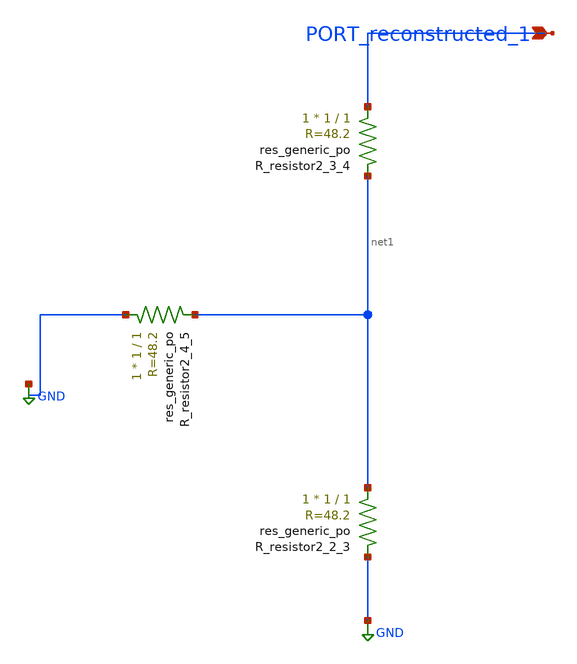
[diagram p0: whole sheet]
** sch_path: schematics/AMSNet/94.sch
**.subckt 94 PORT_reconstructed_1
*.ipin PORT_reconstructed_1
XR_resistor2_2_3 net1 GND sky130_fd_pr__res_generic_po W=1 L=1 m=1
XR_resistor2_3_4 PORT_reconstructed_1 net1 sky130_fd_pr__res_generic_po W=1 L=1 m=1
XR_resistor2_4_5 GND net1 sky130_fd_pr__res_generic_po W=1 L=1 m=1
**.ends
.GLOBAL GND
.end
